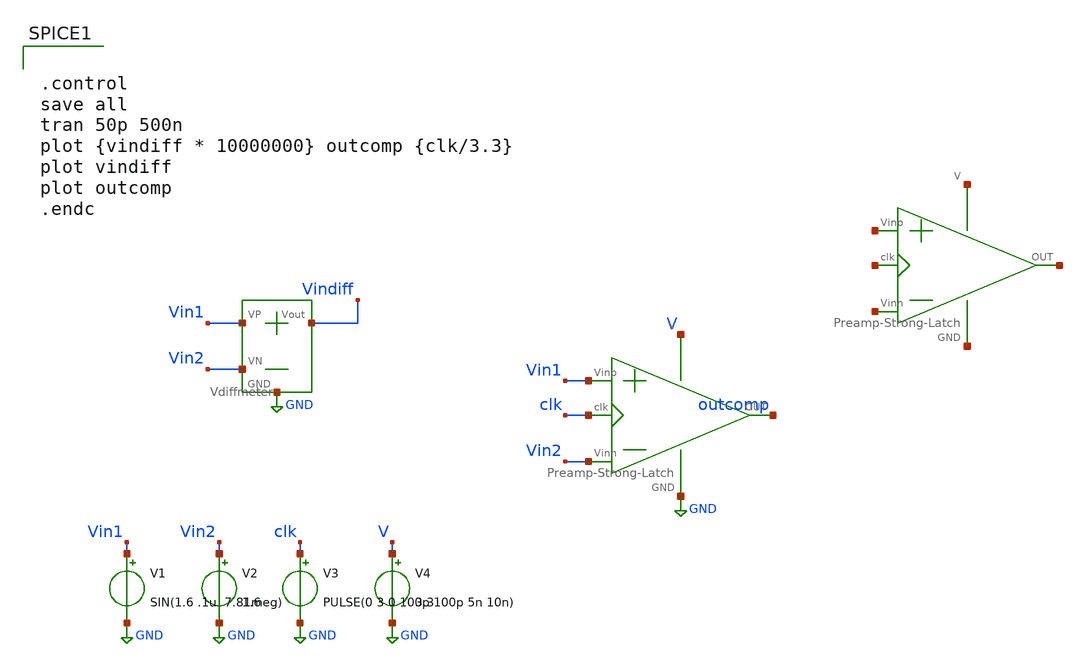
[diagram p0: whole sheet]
** sch_path: SAR_ADC/xschem/test/comp_full_tb/sin_1u_10meg__tb.sch
**.subckt sin_1u_10meg__tb
V1 Vin1 GND SIN(1.6 .1u 7.81meg)
V2 Vin2 GND 1.6
V3 clk GND PULSE(0 3 0 100p 100p 5n 10n)
V4 V GND 3.3
X2 Vin1 Vin2 Vindiff GND Vdiffmeter
X1 V GND Vin1 Vin2 outcomp clk Preamp-Strong-Latch
X3 net1 net2 net3 net4 net5 net6 Preamp-Strong-Latch
**** begin user architecture code


.control
save all
tran 50p 500n
plot {vindiff * 10000000} outcomp {clk/3.3}
plot vindiff
plot outcomp
.endc


.include $env(PDK_ROOT)/$env(PDK)/libs.tech/ngspice/design.ngspice
.lib $env(PDK_ROOT)/$env(PDK)/libs.tech/ngspice/sm141064.ngspice typical

**** end user architecture code
**.ends

* expanding   symbol:  ../../../symbols/Vdiffmeter.sym # of pins=4
** sym_path: SAR_ADC/xschem/spice/symbols/Vdiffmeter.sym
** sch_path: SAR_ADC/xschem/spice/symbols/Vdiffmeter.sch
.subckt Vdiffmeter VP VN Vout GND
*.iopin Vout
*.iopin GND
*.iopin VP
*.iopin VN
R4 Vout GND 1k m=1
E4 Vout GND VP VN 1
.ends


* expanding   symbol:  ../../../symbols/Preamp-Strong-Latch.sym # of pins=6
** sym_path: SAR_ADC/xschem/spice/symbols/Preamp-Strong-Latch.sym
** sch_path: SAR_ADC/xschem/spice/symbols/Preamp-Strong-Latch.sch
.subckt Preamp-Strong-Latch V GND Vinp Vinn OUT clk
*.iopin V
*.iopin GND
*.iopin Vinp
*.iopin Vinn
*.iopin clk
*.iopin OUT
X1 net4 V GND net5 OUT net7 SR_nor
x2 V GND net4 net8 inv cl=0.28u wp=0.44u wn=0.22u
x3 V GND net8 net3 inv cl=0.28u wp=0.44u wn=0.22u
x4 V GND net5 net9 inv cl=0.28u wp=0.44u wn=0.22u
x5 V GND net9 net6 inv cl=0.28u wp=0.44u wn=0.22u
X6 V GND net2 net1 clk net3 net6 strongarm
X7 V GND Vinp clk net1 net2 Vinn preamp
.ends


* expanding   symbol:  symbols/SR_nor.sym # of pins=6
** sym_path: SAR_ADC/xschem/designs/SR_nor.sym
** sch_path: SAR_ADC/xschem/designs/SR_nor.sch
.subckt SR_nor S V GND R Q Qn
*.iopin V
*.iopin GND
*.iopin S
*.iopin R
*.iopin Qn
*.iopin Q
X1 S Q Qn GND V norgate
X2 Qn R Q GND V norgate
.ends


* expanding   symbol:  symbols/inv.sym # of pins=4
** sym_path: SAR_ADC/xschem/spice/inv.sym
** sch_path: SAR_ADC/xschem/spice/inv.sch
.subckt inv vdd gnd vout vin  cl=0.28u wp=0.44u wn=0.22u
*.ipin gnd
*.ipin vdd
*.ipin vin
*.opin vout
XM1 gnd vin vout gnd nfet_03v3 L=0.28u W=4u nf=1 ad='int((nf+1)/2) * W/nf * 0.18u' as='int((nf+2)/2) * W/nf * 0.18u'
+ pd='2*int((nf+1)/2) * (W/nf + 0.18u)' ps='2*int((nf+2)/2) * (W/nf + 0.18u)' nrd='0.18u / W' nrs='0.18u / W'
+ sa=0 sb=0 sd=0 m=1
XM2 vdd vin vout vdd pfet_03v3 L=0.28u W=4u nf=1 ad='int((nf+1)/2) * W/nf * 0.18u' as='int((nf+2)/2) * W/nf * 0.18u'
+ pd='2*int((nf+1)/2) * (W/nf + 0.18u)' ps='2*int((nf+2)/2) * (W/nf + 0.18u)' nrd='0.18u / W' nrs='0.18u / W'
+ sa=0 sb=0 sd=0 m=1
.ends


* expanding   symbol:  symbols/strongarm.sym # of pins=7
** sym_path: SAR_ADC/xschem/designs/strongarm.sym
** sch_path: SAR_ADC/xschem/designs/strongarm.sch
.subckt strongarm V GND Vin1 Vin2 CLK Vout1 Vout2
*.iopin V
*.iopin Vout1
*.iopin Vin1
*.iopin Vin2
*.iopin Vout2
*.iopin CLK
*.iopin GND
XM1 net3 Vout2 V V pfet_03v3 L=0.28u W=2u nf=1 ad='int((nf+1)/2) * W/nf * 0.18u' as='int((nf+2)/2) * W/nf * 0.18u'
+ pd='2*int((nf+1)/2) * (W/nf + 0.18u)' ps='2*int((nf+2)/2) * (W/nf + 0.18u)' nrd='0.18u / W' nrs='0.18u / W'
+ sa=0 sb=0 sd=0 m=1
XM2 Vout1 net1 GND GND nfet_03v3 L=0.28u W=2u nf=1 ad='int((nf+1)/2) * W/nf * 0.18u' as='int((nf+2)/2) * W/nf * 0.18u'
+ pd='2*int((nf+1)/2) * (W/nf + 0.18u)' ps='2*int((nf+2)/2) * (W/nf + 0.18u)' nrd='0.18u / W' nrs='0.18u / W'
+ sa=0 sb=0 sd=0 m=1
XM3 Vout2 Vout1 GND GND nfet_03v3 L=0.28u W=2u nf=1 ad='int((nf+1)/2) * W/nf * 0.18u' as='int((nf+2)/2) * W/nf * 0.18u'
+ pd='2*int((nf+1)/2) * (W/nf + 0.18u)' ps='2*int((nf+2)/2) * (W/nf + 0.18u)' nrd='0.18u / W' nrs='0.18u / W'
+ sa=0 sb=0 sd=0 m=1
XM4 Vout2 net1 GND GND nfet_03v3 L=0.28u W=2u nf=1 ad='int((nf+1)/2) * W/nf * 0.18u' as='int((nf+2)/2) * W/nf * 0.18u'
+ pd='2*int((nf+1)/2) * (W/nf + 0.18u)' ps='2*int((nf+2)/2) * (W/nf + 0.18u)' nrd='0.18u / W' nrs='0.18u / W'
+ sa=0 sb=0 sd=0 m=1
XM5 Vout1 Vout2 GND GND nfet_03v3 L=0.28u W=2u nf=1 ad='int((nf+1)/2) * W/nf * 0.18u' as='int((nf+2)/2) * W/nf * 0.18u'
+ pd='2*int((nf+1)/2) * (W/nf + 0.18u)' ps='2*int((nf+2)/2) * (W/nf + 0.18u)' nrd='0.18u / W' nrs='0.18u / W'
+ sa=0 sb=0 sd=0 m=1
XM6 net2 Vout1 V V pfet_03v3 L=0.28u W=2u nf=1 ad='int((nf+1)/2) * W/nf * 0.18u' as='int((nf+2)/2) * W/nf * 0.18u'
+ pd='2*int((nf+1)/2) * (W/nf + 0.18u)' ps='2*int((nf+2)/2) * (W/nf + 0.18u)' nrd='0.18u / W' nrs='0.18u / W'
+ sa=0 sb=0 sd=0 m=1
XM7 Vout1 Vin1 net3 V pfet_03v3 L=0.28u W=10u nf=1 ad='int((nf+1)/2) * W/nf * 0.18u' as='int((nf+2)/2) * W/nf * 0.18u'
+ pd='2*int((nf+1)/2) * (W/nf + 0.18u)' ps='2*int((nf+2)/2) * (W/nf + 0.18u)' nrd='0.18u / W' nrs='0.18u / W'
+ sa=0 sb=0 sd=0 m=1
XM8 Vout2 Vin2 net2 V pfet_03v3 L=0.28u W=10u nf=1 ad='int((nf+1)/2) * W/nf * 0.18u' as='int((nf+2)/2) * W/nf * 0.18u'
+ pd='2*int((nf+1)/2) * (W/nf + 0.18u)' ps='2*int((nf+2)/2) * (W/nf + 0.18u)' nrd='0.18u / W' nrs='0.18u / W'
+ sa=0 sb=0 sd=0 m=1
x1 V GND net4 CLK inv cl=0.28u wp=0.44u wn=0.22u wx=4u
x2 V GND net1 net4 inv cl=0.28u wp=0.44u wn=0.22u wx=4u
.ends


* expanding   symbol:  symbols/preamp.sym # of pins=7
** sym_path: SAR_ADC/xschem/designs/preamp.sym
** sch_path: SAR_ADC/xschem/designs/preamp.sch
.subckt preamp V GND Vin1 clk Vout1 Vout2 Vin2
*.iopin V
*.iopin GND
*.iopin Vout2
*.iopin Vout1
*.iopin clk
*.iopin Vin2
*.iopin Vin1
XM26 Vout2 clk GND GND nfet_03v3 L=.5u W=.22u nf=1 ad='int((nf+1)/2) * W/nf * 0.18u' as='int((nf+2)/2) * W/nf * 0.18u'
+ pd='2*int((nf+1)/2) * (W/nf + 0.18u)' ps='2*int((nf+2)/2) * (W/nf + 0.18u)' nrd='0.18u / W' nrs='0.18u / W'
+ sa=0 sb=0 sd=0 m=1
XM27 Vout1 clk GND GND nfet_03v3 L=.5u W=.22u nf=1 ad='int((nf+1)/2) * W/nf * 0.18u' as='int((nf+2)/2) * W/nf * 0.18u'
+ pd='2*int((nf+1)/2) * (W/nf + 0.18u)' ps='2*int((nf+2)/2) * (W/nf + 0.18u)' nrd='0.18u / W' nrs='0.18u / W'
+ sa=0 sb=0 sd=0 m=1
XM24 Vout1 Vin2 net1 V pfet_03v3 L=.28u W=8u nf=1 ad='int((nf+1)/2) * W/nf * 0.18u' as='int((nf+2)/2) * W/nf * 0.18u'
+ pd='2*int((nf+1)/2) * (W/nf + 0.18u)' ps='2*int((nf+2)/2) * (W/nf + 0.18u)' nrd='0.18u / W' nrs='0.18u / W'
+ sa=0 sb=0 sd=0 m=1
XM25 Vout2 Vin1 net1 V pfet_03v3 L=.28u W=8u nf=1 ad='int((nf+1)/2) * W/nf * 0.18u' as='int((nf+2)/2) * W/nf * 0.18u'
+ pd='2*int((nf+1)/2) * (W/nf + 0.18u)' ps='2*int((nf+2)/2) * (W/nf + 0.18u)' nrd='0.18u / W' nrs='0.18u / W'
+ sa=0 sb=0 sd=0 m=1
XM1 V clk net1 V pfet_03v3 L=2u W=1u nf=1 ad='int((nf+1)/2) * W/nf * 0.18u' as='int((nf+2)/2) * W/nf * 0.18u'
+ pd='2*int((nf+1)/2) * (W/nf + 0.18u)' ps='2*int((nf+2)/2) * (W/nf + 0.18u)' nrd='0.18u / W' nrs='0.18u / W'
+ sa=0 sb=0 sd=0 m=1
.ends


* expanding   symbol:  norgate.sym # of pins=5
** sym_path: SAR_ADC/xschem/designs/norgate.sym
** sch_path: SAR_ADC/xschem/designs/norgate.sch
.subckt norgate A B Z GND V
*.iopin GND
*.iopin A
*.iopin B
*.iopin V
*.iopin Z
XM3 V A net2 V pfet_03v3 L=0.28u W=0.22u nf=1 ad='int((nf+1)/2) * W/nf * 0.18u' as='int((nf+2)/2) * W/nf * 0.18u'
+ pd='2*int((nf+1)/2) * (W/nf + 0.18u)' ps='2*int((nf+2)/2) * (W/nf + 0.18u)' nrd='0.18u / W' nrs='0.18u / W'
+ sa=0 sb=0 sd=0 m=1
XM6 net2 B Z V pfet_03v3 L=0.28u W=0.22u nf=1 ad='int((nf+1)/2) * W/nf * 0.18u' as='int((nf+2)/2) * W/nf * 0.18u'
+ pd='2*int((nf+1)/2) * (W/nf + 0.18u)' ps='2*int((nf+2)/2) * (W/nf + 0.18u)' nrd='0.18u / W' nrs='0.18u / W'
+ sa=0 sb=0 sd=0 m=1
XM9 V B net1 V pfet_03v3 L=0.28u W=0.22u nf=1 ad='int((nf+1)/2) * W/nf * 0.18u' as='int((nf+2)/2) * W/nf * 0.18u'
+ pd='2*int((nf+1)/2) * (W/nf + 0.18u)' ps='2*int((nf+2)/2) * (W/nf + 0.18u)' nrd='0.18u / W' nrs='0.18u / W'
+ sa=0 sb=0 sd=0 m=1
XM12 net1 A Z V pfet_03v3 L=0.28u W=0.22u nf=1 ad='int((nf+1)/2) * W/nf * 0.18u' as='int((nf+2)/2) * W/nf * 0.18u'
+ pd='2*int((nf+1)/2) * (W/nf + 0.18u)' ps='2*int((nf+2)/2) * (W/nf + 0.18u)' nrd='0.18u / W' nrs='0.18u / W'
+ sa=0 sb=0 sd=0 m=1
XM2 Z B GND GND nfet_03v3 L=0.28u W=0.22u nf=1 ad='int((nf+1)/2) * W/nf * 0.18u' as='int((nf+2)/2) * W/nf * 0.18u'
+ pd='2*int((nf+1)/2) * (W/nf + 0.18u)' ps='2*int((nf+2)/2) * (W/nf + 0.18u)' nrd='0.18u / W' nrs='0.18u / W'
+ sa=0 sb=0 sd=0 m=1
XM4 Z A GND GND nfet_03v3 L=0.28u W=0.22u nf=1 ad='int((nf+1)/2) * W/nf * 0.18u' as='int((nf+2)/2) * W/nf * 0.18u'
+ pd='2*int((nf+1)/2) * (W/nf + 0.18u)' ps='2*int((nf+2)/2) * (W/nf + 0.18u)' nrd='0.18u / W' nrs='0.18u / W'
+ sa=0 sb=0 sd=0 m=1
.ends

.GLOBAL GND
.end
